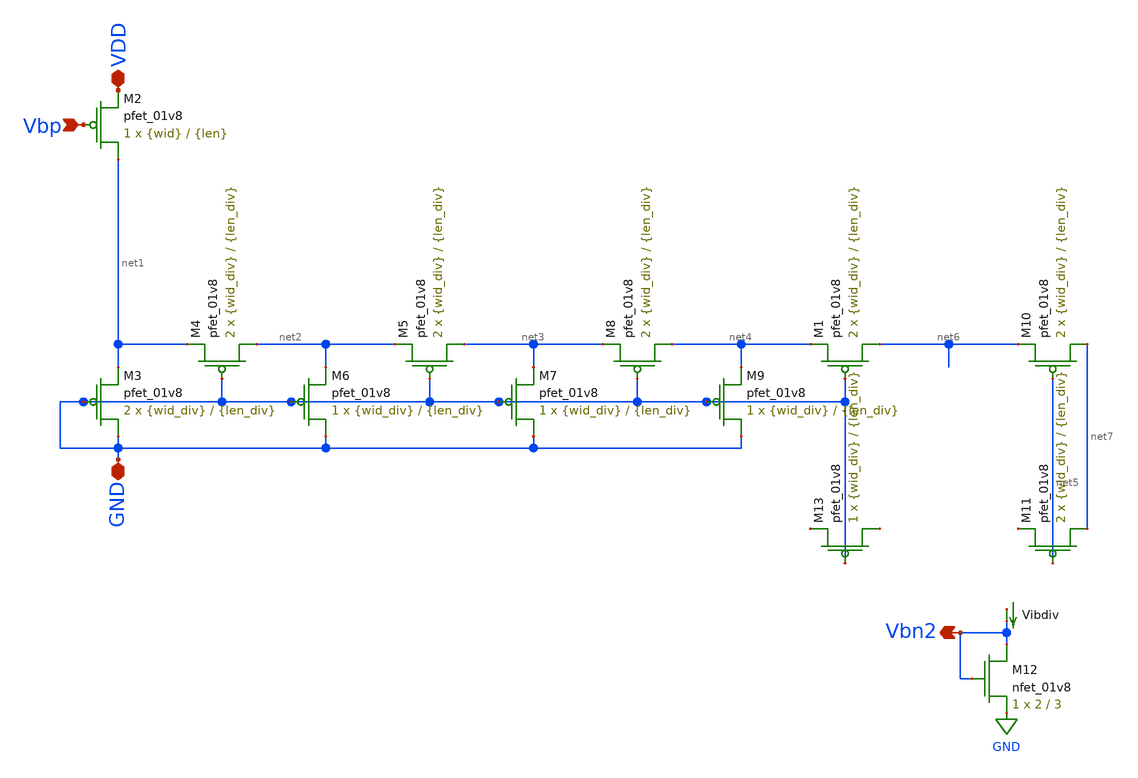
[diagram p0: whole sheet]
** sch_path: mp3/current_divider_lds.sch
**.subckt current_divider_lds GND VDD Vbp Vbn2
*.iopin GND
*.iopin VDD
*.ipin Vbp
*.opin Vbn2
XM2 net1 Vbp VDD VDD sky130_fd_pr__pfet_01v8 L={len} W={wid} nf=1 ad='int((nf+1)/2) * W/nf * 0.29' as='int((nf+2)/2) * W/nf * 0.29'
+ pd='2*int((nf+1)/2) * (W/nf + 0.29)' ps='2*int((nf+2)/2) * (W/nf + 0.29)' nrd='0.29 / W' nrs='0.29 / W'
+ sa=0 sb=0 sd=0 mult=1 m=1
XM3 GND GND net1 VDD sky130_fd_pr__pfet_01v8 L={len_div} W={wid_div} nf=1 ad='int((nf+1)/2) * W/nf * 0.29'
+ as='int((nf+2)/2) * W/nf * 0.29' pd='2*int((nf+1)/2) * (W/nf + 0.29)' ps='2*int((nf+2)/2) * (W/nf + 0.29)'
+ nrd='0.29 / W' nrs='0.29 / W' sa=0 sb=0 sd=0 mult=2 m=2
XM4 net2 GND net1 VDD sky130_fd_pr__pfet_01v8 L={len_div} W={wid_div} nf=1 ad='int((nf+1)/2) * W/nf * 0.29'
+ as='int((nf+2)/2) * W/nf * 0.29' pd='2*int((nf+1)/2) * (W/nf + 0.29)' ps='2*int((nf+2)/2) * (W/nf + 0.29)'
+ nrd='0.29 / W' nrs='0.29 / W' sa=0 sb=0 sd=0 mult=2 m=2
XM6 GND GND net2 VDD sky130_fd_pr__pfet_01v8 L={len_div} W={wid_div} nf=1 ad='int((nf+1)/2) * W/nf * 0.29'
+ as='int((nf+2)/2) * W/nf * 0.29' pd='2*int((nf+1)/2) * (W/nf + 0.29)' ps='2*int((nf+2)/2) * (W/nf + 0.29)'
+ nrd='0.29 / W' nrs='0.29 / W' sa=0 sb=0 sd=0 mult=1 m=1
XM5 net3 GND net2 VDD sky130_fd_pr__pfet_01v8 L={len_div} W={wid_div} nf=1 ad='int((nf+1)/2) * W/nf * 0.29'
+ as='int((nf+2)/2) * W/nf * 0.29' pd='2*int((nf+1)/2) * (W/nf + 0.29)' ps='2*int((nf+2)/2) * (W/nf + 0.29)'
+ nrd='0.29 / W' nrs='0.29 / W' sa=0 sb=0 sd=0 mult=2 m=2
XM7 GND GND net3 VDD sky130_fd_pr__pfet_01v8 L={len_div} W={wid_div} nf=1 ad='int((nf+1)/2) * W/nf * 0.29'
+ as='int((nf+2)/2) * W/nf * 0.29' pd='2*int((nf+1)/2) * (W/nf + 0.29)' ps='2*int((nf+2)/2) * (W/nf + 0.29)'
+ nrd='0.29 / W' nrs='0.29 / W' sa=0 sb=0 sd=0 mult=1 m=1
XM8 net4 GND net3 VDD sky130_fd_pr__pfet_01v8 L={len_div} W={wid_div} nf=1 ad='int((nf+1)/2) * W/nf * 0.29'
+ as='int((nf+2)/2) * W/nf * 0.29' pd='2*int((nf+1)/2) * (W/nf + 0.29)' ps='2*int((nf+2)/2) * (W/nf + 0.29)'
+ nrd='0.29 / W' nrs='0.29 / W' sa=0 sb=0 sd=0 mult=2 m=2
XM9 GND GND net4 VDD sky130_fd_pr__pfet_01v8 L={len_div} W={wid_div} nf=1 ad='int((nf+1)/2) * W/nf * 0.29'
+ as='int((nf+2)/2) * W/nf * 0.29' pd='2*int((nf+1)/2) * (W/nf + 0.29)' ps='2*int((nf+2)/2) * (W/nf + 0.29)'
+ nrd='0.29 / W' nrs='0.29 / W' sa=0 sb=0 sd=0 mult=1 m=1
XM10 net7 net5 net6 VDD sky130_fd_pr__pfet_01v8 L={len_div} W={wid_div} nf=1 ad='int((nf+1)/2) * W/nf * 0.29'
+ as='int((nf+2)/2) * W/nf * 0.29' pd='2*int((nf+1)/2) * (W/nf + 0.29)' ps='2*int((nf+2)/2) * (W/nf + 0.29)'
+ nrd='0.29 / W' nrs='0.29 / W' sa=0 sb=0 sd=0 mult=2 m=2
XM11 net7 net5 net8 VDD sky130_fd_pr__pfet_01v8 L={len_div} W={wid_div} nf=1 ad='int((nf+1)/2) * W/nf * 0.29'
+ as='int((nf+2)/2) * W/nf * 0.29' pd='2*int((nf+1)/2) * (W/nf + 0.29)' ps='2*int((nf+2)/2) * (W/nf + 0.29)'
+ nrd='0.29 / W' nrs='0.29 / W' sa=0 sb=0 sd=0 mult=2 m=2
XM12 Vbn2 Vbn2 GND GND sky130_fd_pr__nfet_01v8 L=3 W=2 nf=1 ad='int((nf+1)/2) * W/nf * 0.29' as='int((nf+2)/2) * W/nf * 0.29'
+ pd='2*int((nf+1)/2) * (W/nf + 0.29)' ps='2*int((nf+2)/2) * (W/nf + 0.29)' nrd='0.29 / W' nrs='0.29 / W'
+ sa=0 sb=0 sd=0 mult=1 m=1
Vibdiv net9 Vbn2 0
.save i(vibdiv)
XM1 net6 GND net4 VDD sky130_fd_pr__pfet_01v8 L={len_div} W={wid_div} nf=1 ad='int((nf+1)/2) * W/nf * 0.29'
+ as='int((nf+2)/2) * W/nf * 0.29' pd='2*int((nf+1)/2) * (W/nf + 0.29)' ps='2*int((nf+2)/2) * (W/nf + 0.29)'
+ nrd='0.29 / W' nrs='0.29 / W' sa=0 sb=0 sd=0 mult=2 m=2
XM13 net10 GND net11 VDD sky130_fd_pr__pfet_01v8 L={len_div} W={wid_div} nf=1 ad='int((nf+1)/2) * W/nf * 0.29'
+ as='int((nf+2)/2) * W/nf * 0.29' pd='2*int((nf+1)/2) * (W/nf + 0.29)' ps='2*int((nf+2)/2) * (W/nf + 0.29)'
+ nrd='0.29 / W' nrs='0.29 / W' sa=0 sb=0 sd=0 mult=1 m=1
**.ends
.GLOBAL GND
.end
